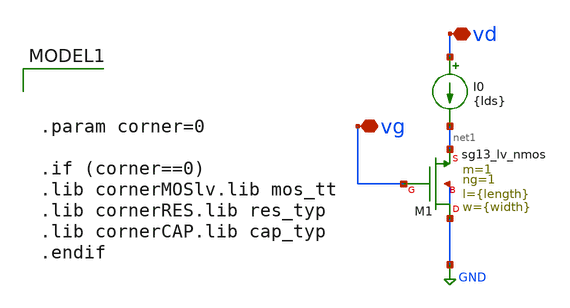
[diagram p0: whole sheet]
** sch_path: Tarea1/xschem/Width_sweep.sch
**.subckt Width_sweep vg vd
*.iopin vg
*.iopin vd
XM1 GND vg net1 GND sg13_lv_nmos w={width} l={length} ng=1 m=1 mm_ok=1
I0 vd net1 {Ids}
**** begin user architecture code


.param corner=0

.if (corner==0)
.lib cornerMOSlv.lib mos_tt
.lib cornerRES.lib res_typ
.lib cornerCAP.lib cap_typ
.endif



.option wnflag=1
*vsup VDD 0 1.8
vin vg 0 0.35
vds vd 0 1.8
.param length = 0.5u
.param width = 4.38u
.param Ids = {120u*3.1415}
cload vd 0 5p

.control
let strt_w = 0.3u
let stop_w = 3u
let step_w = 0.05u
let curr_w = strt_w

shell rm -f gmid_sweep_w.raw
shell rm -f vov_sweep_w.raw

while curr_w le stop_w
    alterparam length = $&curr_w
    reset
    save all
    save @n.xm1.nsg13_lv_nmos[gm]
    save @n.xm1.nsg13_lv_nmos[ids]
    dc vin 0.35 0.35 0.01
    let idn = @n.xm1.nsg13_lv_nmos[ids]
    let gm  = @n.xm1.nsg13_lv_nmos[gm]
    let gmid= gm/idn
    let idw = idn/curr_w
    set appendwrite
    wrdata gmid_sweep_w.raw gmid idw


    let curr_w = curr_w + step_w
end
.endc



**** end user architecture code
**.ends
.GLOBAL GND
.end
